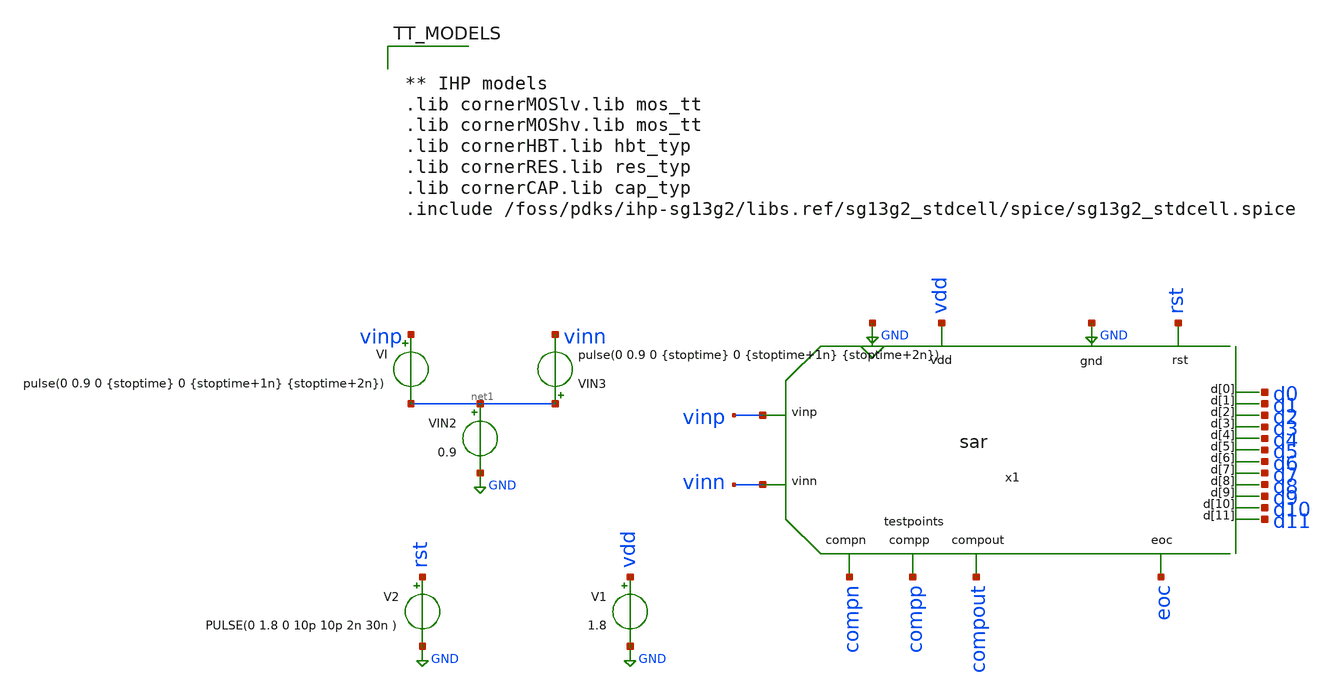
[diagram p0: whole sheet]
** sch_path: xschem/SAR_ADC/testbench/tb_sar_adc_rampa.sch
**.subckt tb_sar_adc_rampa
x1 vinp rst GND vinn GND vdd compn compp compout eoc d9 d7 d0 d11 d3 d4 d2 d1 d8 d6 d5 d10 sar
VI vinp net1 pulse(0 0.9 0 {stoptime} 0 {stoptime+1n} {stoptime+2n})
V1 vdd GND 1.8
VIN2 net1 GND 0.9
VIN3 net1 vinn pulse(0 0.9 0 {stoptime} 0 {stoptime+1n} {stoptime+2n})
V2 rst GND PULSE(0 1.8 0 10p 10p 2n 30n )
**** begin user architecture code


.param periodclk=2n
.param periodconv=30n
.param stoptime=2*periodconv
.param ro = 300

.options klu method=gear reltol=1e-2 abstol=1e-15 gmin=1e-15


.tran {0.01*periodclk} {stoptime}
.save time V(d0) V(d1) V(d2) V(d3) V(d4) V(d5) V(d6) V(d7) V(d8) V(d9) V(d10) V(d11) vinp vinn eoc rst compout compp compn x1.comp_clk
.control
run

*plot {(V(d11)*2+V(d10)*4+V(d9)*8+V(d8)*16+V(d7)*32+V(d6)*64+V(d5)*128+V(d4)*256+V(d3)*512+V(d2)*1024+V(d1)*2048)/4096}
*+ {2*rst} eoc {vinp - vinn}
*plot {(V(d11)*2+V(d10)*4+V(d9)*8+V(d8)*16+V(d7)*32+V(d6)*64+V(d5)*128+V(d4)*256+V(d3)*512+V(d2)*1024+V(d1)*2048-V(d0)*4096)/4096}
*+ {2*rst} eoc {vinp - vinn}
*plot {(-V(d0)*2048 + V(d1)*1024 + V(d2)*512 + V(d3)*256 + V(d4)*128 + V(d5)*64 + V(d6)*32 + V(d7)*16 + V(d8)*8 + V(d9)*4 + V(d10)*2 + V(d11))/2048}
plot {((V(d0)-1.8)*2048 + V(d1)*1024 + V(d2)*512 + V(d3)*256 + V(d4)*128 + V(d5)*64 + V(d6)*32 + V(d7)*16 + V(d8)*8 + V(d9)*4 + V(d10)*2 + V(d11))/2048}
+ rst eoc vinp-vinn
plot compp compn {compout + 4}
plot {d0} {d1 + 4} {d2 + 8} {d3 + 12} {d4 + 16} {d5 + 20} {d6 + 24} {d7 + 28} {d8 + 32} {d9 + 36} {d10 + 40}
+ {d11 + 44} {x1.comp_clk + 50} {compout + 55} {eoc + 60}  {compp - compn - 2}
plot compp-compn x1.comp_clk compout

*wrdata adc_signals.csv time V(d0) V(d1) V(d2) V(d3) V(d4) V(d5) V(d6) V(d7) V(d8) V(d9) V(d10)
*+ V(d11) vinp vinn eoc rst compout compp compn x1.comp_clk
write adc_signals.raw time V(d0) V(d1) V(d2) V(d3) V(d4) V(d5) V(d6) V(d7) V(d8) V(d9) V(d10) V(d11)
+ vinp vinn eoc rst compout compp compn x1.comp_clk
quit
.endc




** IHP models
.lib cornerMOSlv.lib mos_tt
.lib cornerMOShv.lib mos_tt
.lib cornerHBT.lib hbt_typ
.lib cornerRES.lib res_typ
.lib cornerCAP.lib cap_typ
.include /foss/pdks/ihp-sg13g2/libs.ref/sg13g2_stdcell/spice/sg13g2_stdcell.spice


**** end user architecture code
**.ends
.GLOBAL GND
.end
